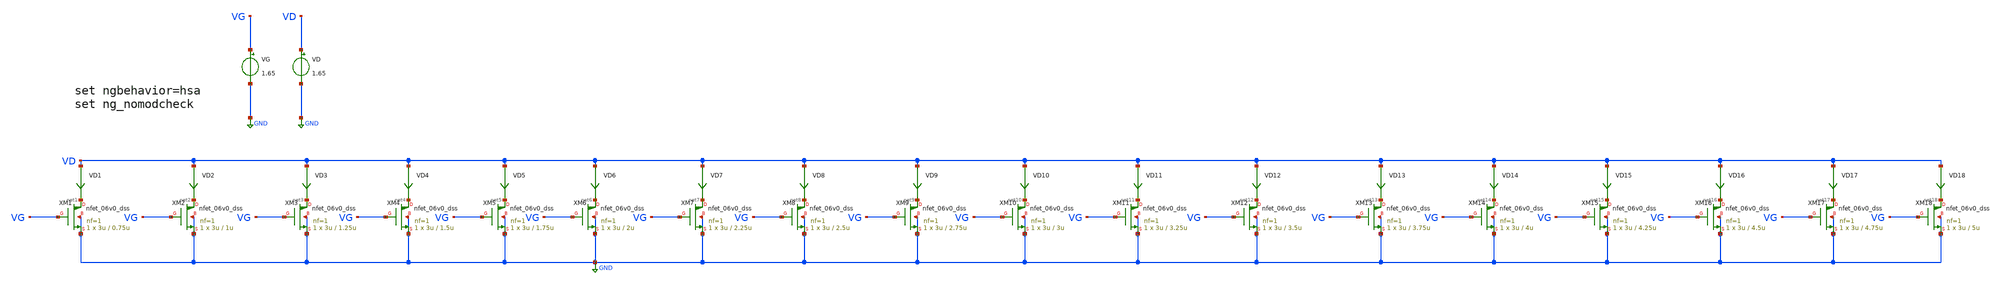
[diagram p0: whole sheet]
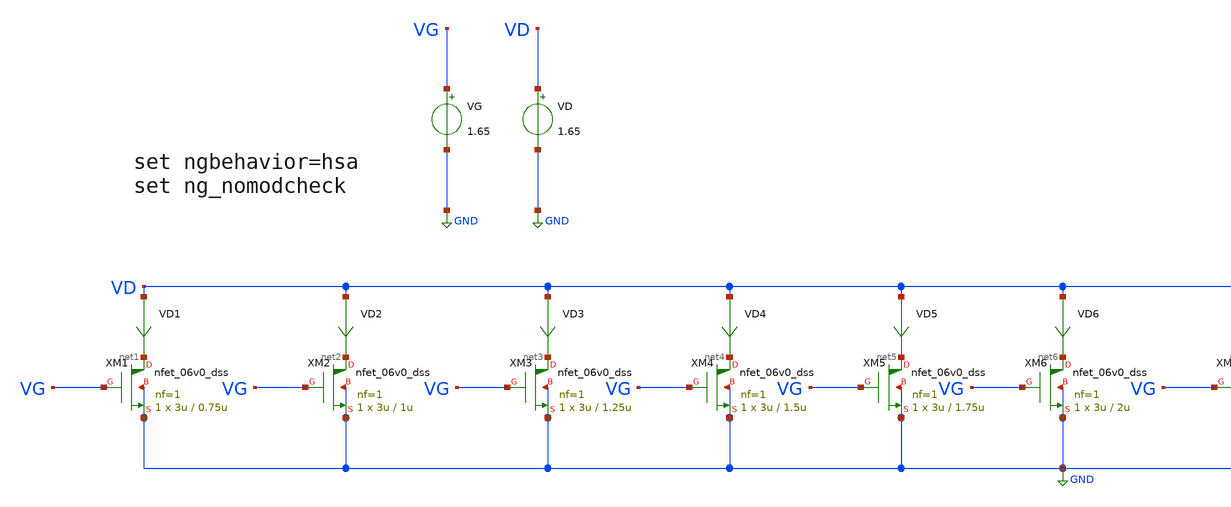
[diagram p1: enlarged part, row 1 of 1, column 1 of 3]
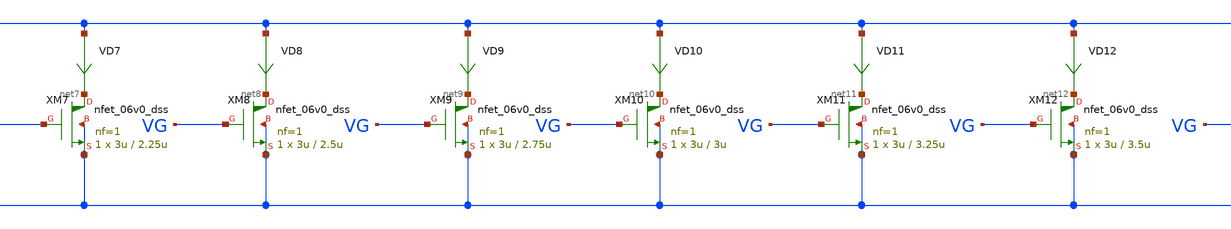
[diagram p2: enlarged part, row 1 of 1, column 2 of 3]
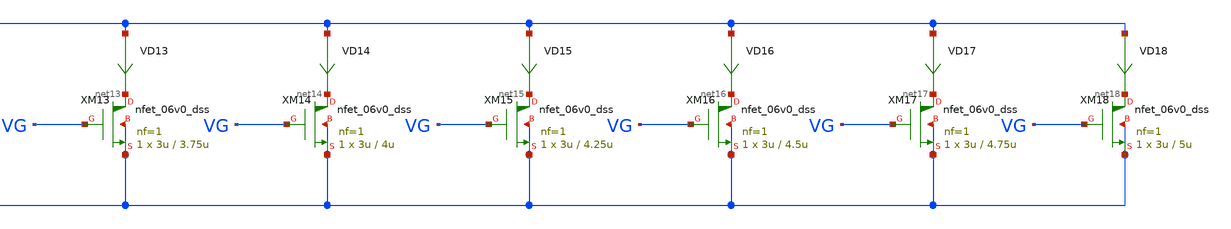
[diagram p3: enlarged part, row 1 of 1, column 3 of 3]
** sch_path: Design-Files/gmid_nmos_06v0_dss.sch
**.subckt gmid_nmos_06v0_dss
VG VG GND 1.65
VD VD GND 1.65
VD1 VD net1 0
.save i(vd1)
VD2 VD net2 0
.save i(vd2)
VD3 VD net3 0
.save i(vd3)
VD4 VD net4 0
.save i(vd4)
VD5 VD net5 0
.save i(vd5)
VD6 VD net6 0
.save i(vd6)
VD7 VD net7 0
.save i(vd7)
VD8 VD net8 0
.save i(vd8)
VD9 VD net9 0
.save i(vd9)
VD10 VD net10 0
.save i(vd10)
VD11 VD net11 0
.save i(vd11)
VD12 VD net12 0
.save i(vd12)
XM1 net1 VG GND GND nfet_06v0_dss L=0.75u W=3u nf=1 ad='int((nf+1)/2) * W/nf * 0.18u' as='int((nf+2)/2) * W/nf * 0.18u'
+ pd='2*int((nf+1)/2) * (W/nf + 0.18u)' ps='2*int((nf+2)/2) * (W/nf + 0.18u)' nrd='0.18u / W' nrs='0.18u / W'
+ sa=0 sb=0 sd=0 m=1
XM2 net2 VG GND GND nfet_06v0_dss L=1u W=3u nf=1 ad='int((nf+1)/2) * W/nf * 0.18u' as='int((nf+2)/2) * W/nf * 0.18u'
+ pd='2*int((nf+1)/2) * (W/nf + 0.18u)' ps='2*int((nf+2)/2) * (W/nf + 0.18u)' nrd='0.18u / W' nrs='0.18u / W'
+ sa=0 sb=0 sd=0 m=1
XM3 net3 VG GND GND nfet_06v0_dss L=1.25u W=3u nf=1 ad='int((nf+1)/2) * W/nf * 0.18u' as='int((nf+2)/2) * W/nf * 0.18u'
+ pd='2*int((nf+1)/2) * (W/nf + 0.18u)' ps='2*int((nf+2)/2) * (W/nf + 0.18u)' nrd='0.18u / W' nrs='0.18u / W'
+ sa=0 sb=0 sd=0 m=1
XM4 net4 VG GND GND nfet_06v0_dss L=1.5u W=3u nf=1 ad='int((nf+1)/2) * W/nf * 0.18u' as='int((nf+2)/2) * W/nf * 0.18u'
+ pd='2*int((nf+1)/2) * (W/nf + 0.18u)' ps='2*int((nf+2)/2) * (W/nf + 0.18u)' nrd='0.18u / W' nrs='0.18u / W'
+ sa=0 sb=0 sd=0 m=1
XM5 net5 VG GND GND nfet_06v0_dss L=1.75u W=3u nf=1 ad='int((nf+1)/2) * W/nf * 0.18u' as='int((nf+2)/2) * W/nf * 0.18u'
+ pd='2*int((nf+1)/2) * (W/nf + 0.18u)' ps='2*int((nf+2)/2) * (W/nf + 0.18u)' nrd='0.18u / W' nrs='0.18u / W'
+ sa=0 sb=0 sd=0 m=1
XM6 net6 VG GND GND nfet_06v0_dss L=2u W=3u nf=1 ad='int((nf+1)/2) * W/nf * 0.18u' as='int((nf+2)/2) * W/nf * 0.18u'
+ pd='2*int((nf+1)/2) * (W/nf + 0.18u)' ps='2*int((nf+2)/2) * (W/nf + 0.18u)' nrd='0.18u / W' nrs='0.18u / W'
+ sa=0 sb=0 sd=0 m=1
XM7 net7 VG GND GND nfet_06v0_dss L=2.25u W=3u nf=1 ad='int((nf+1)/2) * W/nf * 0.18u' as='int((nf+2)/2) * W/nf * 0.18u'
+ pd='2*int((nf+1)/2) * (W/nf + 0.18u)' ps='2*int((nf+2)/2) * (W/nf + 0.18u)' nrd='0.18u / W' nrs='0.18u / W'
+ sa=0 sb=0 sd=0 m=1
XM8 net8 VG GND GND nfet_06v0_dss L=2.5u W=3u nf=1 ad='int((nf+1)/2) * W/nf * 0.18u' as='int((nf+2)/2) * W/nf * 0.18u'
+ pd='2*int((nf+1)/2) * (W/nf + 0.18u)' ps='2*int((nf+2)/2) * (W/nf + 0.18u)' nrd='0.18u / W' nrs='0.18u / W'
+ sa=0 sb=0 sd=0 m=1
XM9 net9 VG GND GND nfet_06v0_dss L=2.75u W=3u nf=1 ad='int((nf+1)/2) * W/nf * 0.18u' as='int((nf+2)/2) * W/nf * 0.18u'
+ pd='2*int((nf+1)/2) * (W/nf + 0.18u)' ps='2*int((nf+2)/2) * (W/nf + 0.18u)' nrd='0.18u / W' nrs='0.18u / W'
+ sa=0 sb=0 sd=0 m=1
XM10 net10 VG GND GND nfet_06v0_dss L=3u W=3u nf=1 ad='int((nf+1)/2) * W/nf * 0.18u' as='int((nf+2)/2) * W/nf * 0.18u'
+ pd='2*int((nf+1)/2) * (W/nf + 0.18u)' ps='2*int((nf+2)/2) * (W/nf + 0.18u)' nrd='0.18u / W' nrs='0.18u / W'
+ sa=0 sb=0 sd=0 m=1
XM11 net11 VG GND GND nfet_06v0_dss L=3.25u W=3u nf=1 ad='int((nf+1)/2) * W/nf * 0.18u' as='int((nf+2)/2) * W/nf * 0.18u'
+ pd='2*int((nf+1)/2) * (W/nf + 0.18u)' ps='2*int((nf+2)/2) * (W/nf + 0.18u)' nrd='0.18u / W' nrs='0.18u / W'
+ sa=0 sb=0 sd=0 m=1
XM12 net12 VG GND GND nfet_06v0_dss L=3.5u W=3u nf=1 ad='int((nf+1)/2) * W/nf * 0.18u' as='int((nf+2)/2) * W/nf * 0.18u'
+ pd='2*int((nf+1)/2) * (W/nf + 0.18u)' ps='2*int((nf+2)/2) * (W/nf + 0.18u)' nrd='0.18u / W' nrs='0.18u / W'
+ sa=0 sb=0 sd=0 m=1
VD13 VD net13 0
.save i(vd13)
VD14 VD net14 0
.save i(vd14)
VD15 VD net15 0
.save i(vd15)
VD16 VD net16 0
.save i(vd16)
VD17 VD net17 0
.save i(vd17)
VD18 VD net18 0
.save i(vd18)
XM13 net13 VG GND GND nfet_06v0_dss L=3.75u W=3u nf=1 ad='int((nf+1)/2) * W/nf * 0.18u' as='int((nf+2)/2) * W/nf * 0.18u'
+ pd='2*int((nf+1)/2) * (W/nf + 0.18u)' ps='2*int((nf+2)/2) * (W/nf + 0.18u)' nrd='0.18u / W' nrs='0.18u / W'
+ sa=0 sb=0 sd=0 m=1
XM14 net14 VG GND GND nfet_06v0_dss L=4u W=3u nf=1 ad='int((nf+1)/2) * W/nf * 0.18u' as='int((nf+2)/2) * W/nf * 0.18u'
+ pd='2*int((nf+1)/2) * (W/nf + 0.18u)' ps='2*int((nf+2)/2) * (W/nf + 0.18u)' nrd='0.18u / W' nrs='0.18u / W'
+ sa=0 sb=0 sd=0 m=1
XM15 net15 VG GND GND nfet_06v0_dss L=4.25u W=3u nf=1 ad='int((nf+1)/2) * W/nf * 0.18u' as='int((nf+2)/2) * W/nf * 0.18u'
+ pd='2*int((nf+1)/2) * (W/nf + 0.18u)' ps='2*int((nf+2)/2) * (W/nf + 0.18u)' nrd='0.18u / W' nrs='0.18u / W'
+ sa=0 sb=0 sd=0 m=1
XM16 net16 VG GND GND nfet_06v0_dss L=4.5u W=3u nf=1 ad='int((nf+1)/2) * W/nf * 0.18u' as='int((nf+2)/2) * W/nf * 0.18u'
+ pd='2*int((nf+1)/2) * (W/nf + 0.18u)' ps='2*int((nf+2)/2) * (W/nf + 0.18u)' nrd='0.18u / W' nrs='0.18u / W'
+ sa=0 sb=0 sd=0 m=1
XM17 net17 VG GND GND nfet_06v0_dss L=4.75u W=3u nf=1 ad='int((nf+1)/2) * W/nf * 0.18u' as='int((nf+2)/2) * W/nf * 0.18u'
+ pd='2*int((nf+1)/2) * (W/nf + 0.18u)' ps='2*int((nf+2)/2) * (W/nf + 0.18u)' nrd='0.18u / W' nrs='0.18u / W'
+ sa=0 sb=0 sd=0 m=1
XM18 net18 VG GND GND nfet_06v0_dss L=5u W=3u nf=1 ad='int((nf+1)/2) * W/nf * 0.18u' as='int((nf+2)/2) * W/nf * 0.18u'
+ pd='2*int((nf+1)/2) * (W/nf + 0.18u)' ps='2*int((nf+2)/2) * (W/nf + 0.18u)' nrd='0.18u / W' nrs='0.18u / W'
+ sa=0 sb=0 sd=0 m=1
**** begin user architecture code


* ngspice commands
.option wnflag=1
.option .savecurrents
.control
save all
dc VG 0.05 6 0.1m
** remove zero length vectors to prevent write errors
remzerovec
write /foss/designs/PDK-CHAR/GF180-MCUD/NMOS_06v6_DSS/gmid_nmos_03v3_dss_tb.raw

plot @m.xm1.m0[gm]
plot @m.xm2.m0[gm]
plot @m.xm3.m0[gm]
plot @m.xm4.m0[gm]
plot @m.xm5.m0[gm]
plot @m.xm6.m0[gm]
plot @m.xm7.m0[gm]
plot @m.xm8.m0[gm]
plot @m.xm9.m0[gm]
plot @m.xm10.m0[gm]
plot @m.xm11.m0[gm]
plot @m.xm12.m0[gm]
plot @m.xm13.m0[gm]
plot @m.xm14.m0[gm]
plot @m.xm15.m0[gm]
plot @m.xm16.m0[gm]
plot @m.xm17.m0[gm]
plot @m.xm18.m0[gm]


wrdata /foss/designs/PDK-CHAR/GF180-MCUD/NMOS_06v0_DSS/gmid_nmos_1_nfet_03v3_dss_tb.txt
+ @m.xm1.m0[gm] i(VD1) @m.xm1.m0[vth] @m.xm1.m0[gds] @m.xm1.m0[cgg] @m.xm1.m0[cgs] @m.xm1.m0[cgd]
wrdata /foss/designs/PDK-CHAR/GF180-MCUD/NMOS_06v0_DSS/gmid_nmos_2_nfet_03v3_dss_tb.txt
+ @m.xm2.m0[gm] i(VD2) @m.xm2.m0[vth] @m.xm2.m0[gds] @m.xm2.m0[cgg] @m.xm2.m0[cgs] @m.xm2.m0[cgd]
wrdata /foss/designs/PDK-CHAR/GF180-MCUD/NMOS_06v0_DSS/gmid_nmos_3_nfet_03v3_dss_tb.txt
+ @m.xm3.m0[gm] i(VD3) @m.xm3.m0[vth] @m.xm3.m0[gds] @m.xm3.m0[cgg] @m.xm3.m0[cgs] @m.xm3.m0[cgd]
wrdata /foss/designs/PDK-CHAR/GF180-MCUD/NMOS_06v0_DSS/gmid_nmos_4_nfet_03v3_dss_tb.txt
+ @m.xm4.m0[gm] i(VD4) @m.xm4.m0[vth] @m.xm4.m0[gds] @m.xm4.m0[cgg] @m.xm4.m0[cgs] @m.xm4.m0[cgd]
wrdata /foss/designs/PDK-CHAR/GF180-MCUD/NMOS_06v0_DSS/gmid_nmos_5_nfet_03v3_dss_tb.txt
+ @m.xm5.m0[gm] i(VD5) @m.xm5.m0[vth] @m.xm5.m0[gds] @m.xm5.m0[cgg] @m.xm5.m0[cgs] @m.xm5.m0[cgd]
wrdata /foss/designs/PDK-CHAR/GF180-MCUD/NMOS_06v0_DSS/gmid_nmos_6_nfet_03v3_dss_tb.txt
+ @m.xm6.m0[gm] i(VD6) @m.xm6.m0[vth] @m.xm6.m0[gds] @m.xm6.m0[cgg] @m.xm6.m0[cgs] @m.xm6.m0[cgd]
wrdata /foss/designs/PDK-CHAR/GF180-MCUD/NMOS_06v0_DSS/gmid_nmos_7_nfet_03v3_dss_tb.txt
+ @m.xm7.m0[gm] i(VD7) @m.xm7.m0[vth] @m.xm7.m0[gds] @m.xm7.m0[cgg] @m.xm7.m0[cgs] @m.xm7.m0[cgd]
wrdata /foss/designs/PDK-CHAR/GF180-MCUD/NMOS_06v0_DSS/gmid_nmos_8_nfet_03v3_dss_tb.txt
+ @m.xm8.m0[gm] i(VD8) @m.xm8.m0[vth] @m.xm8.m0[gds] @m.xm8.m0[cgg] @m.xm8.m0[cgs] @m.xm8.m0[cgd]
wrdata /foss/designs/PDK-CHAR/GF180-MCUD/NMOS_06v0_DSS/gmid_nmos_9_nfet_03v3_dss_tb.txt
+ @m.xm9.m0[gm] i(VD9) @m.xm9.m0[vth] @m.xm9.m0[gds] @m.xm9.m0[cgg] @m.xm9.m0[cgs] @m.xm9.m0[cgd]
wrdata /foss/designs/PDK-CHAR/GF180-MCUD/NMOS_06v0_DSS/gmid_nmos_10_nfet_03v3_dss_tb.txt
+ @m.xm10.m0[gm] i(VD10) @m.xm10.m0[vth] @m.xm10.m0[gds] @m.xm10.m0[cgg] @m.xm10.m0[cgs] @m.xm10.m0[cgd]
wrdata /foss/designs/PDK-CHAR/GF180-MCUD/NMOS_06v0_DSS/gmid_nmos_11_nfet_03v3_dss_tb.txt
+ @m.xm11.m0[gm] i(VD11) @m.xm11.m0[vth] @m.xm11.m0[gds] @m.xm11.m0[cgg] @m.xm11.m0[cgs] @m.xm11.m0[cgd]
wrdata /foss/designs/PDK-CHAR/GF180-MCUD/NMOS_06v0_DSS/gmid_nmos_12_nfet_03v3_dss_tb.txt
+ @m.xm12.m0[gm] i(VD12) @m.xm12.m0[vth] @m.xm12.m0[gds] @m.xm12.m0[cgg] @m.xm12.m0[cgs] @m.xm12.m0[cgd]
wrdata /foss/designs/PDK-CHAR/GF180-MCUD/NMOS_06v0_DSS/gmid_nmos_13_nfet_03v3_dss_tb.txt
+ @m.xm13.m0[gm] i(VD13) @m.xm13.m0[vth] @m.xm13.m0[gds] @m.xm13.m0[cgg] @m.xm13.m0[cgs] @m.xm13.m0[cgd]
wrdata /foss/designs/PDK-CHAR/GF180-MCUD/NMOS_06v0_DSS/gmid_nmos_14_nfet_03v3_dss_tb.txt
+ @m.xm14.m0[gm] i(VD14) @m.xm14.m0[vth] @m.xm14.m0[gds] @m.xm14.m0[cgg] @m.xm14.m0[cgs] @m.xm14.m0[cgd]
wrdata /foss/designs/PDK-CHAR/GF180-MCUD/NMOS_06v0_DSS/gmid_nmos_15_nfet_03v3_dss_tb.txt
+ @m.xm15.m0[gm] i(VD15) @m.xm15.m0[vth] @m.xm15.m0[gds] @m.xm15.m0[cgg] @m.xm15.m0[cgs] @m.xm15.m0[cgd]
wrdata /foss/designs/PDK-CHAR/GF180-MCUD/NMOS_06v0_DSS/gmid_nmos_16_nfet_03v3_dss_tb.txt
+ @m.xm16.m0[gm] i(VD13) @m.xm16.m0[vth] @m.xm16.m0[gds] @m.xm16.m0[cgg] @m.xm16.m0[cgs] @m.xm16.m0[cgd]
wrdata /foss/designs/PDK-CHAR/GF180-MCUD/NMOS_06v0_DSS/gmid_nmos_17_nfet_03v3_dss_tb.txt
+ @m.xm17.m0[gm] i(VD14) @m.xm17.m0[vth] @m.xm17.m0[gds] @m.xm17.m0[cgg] @m.xm17.m0[cgs] @m.xm17.m0[cgd]
wrdata /foss/designs/PDK-CHAR/GF180-MCUD/NMOS_06v0_DSS/gmid_nmos_18_nfet_03v3_dss_tb.txt
+ @m.xm18.m0[gm] i(VD15) @m.xm18.m0[vth] @m.xm18.m0[gds] @m.xm18.m0[cgg] @m.xm18.m0[cgs] @m.xm18.m0[cgd]
set appendwrite
op
remzerovec
write /foss/designs/PDK-CHAR/GF180-MCUD/NMOS_06v6_DSS/gmid_nmos_03v3_dss_tb.raw
**quit 0
.endc




.save @m.xm1.m0[gm]
.save @m.xm1.m0[vth]
.save @m.xm1.m0[gds]
.save @m.xm1.m0[cgg]
.save @m.xm1.m0[cgs]
.save @m.xm1.m0[cgd]
.save @m.xm2.m0[gm]
.save @m.xm2.m0[vth]
.save @m.xm2.m0[gds]
.save @m.xm2.m0[cgg]
.save @m.xm2.m0[cgs]
.save @m.xm2.m0[cgd]
.save @m.xm3.m0[gm]
.save @m.xm3.m0[vth]
.save @m.xm3.m0[gds]
.save @m.xm3.m0[cgg]
.save @m.xm3.m0[cgs]
.save @m.xm3.m0[cgd]
.save @m.xm4.m0[gm]
.save @m.xm4.m0[vth]
.save @m.xm4.m0[gds]
.save @m.xm4.m0[cgg]
.save @m.xm4.m0[cgs]
.save @m.xm4.m0[cgd]
.save @m.xm5.m0[gm]
.save @m.xm5.m0[vth]
.save @m.xm5.m0[gds]
.save @m.xm5.m0[cgg]
.save @m.xm5.m0[cgs]
.save @m.xm5.m0[cgd]
.save @m.xm6.m0[gm]
.save @m.xm6.m0[vth]
.save @m.xm6.m0[gds]
.save @m.xm6.m0[cgg]
.save @m.xm6.m0[cgs]
.save @m.xm6.m0[cgd]
.save @m.xm7.m0[gm]
.save @m.xm7.m0[vth]
.save @m.xm7.m0[gds]
.save @m.xm7.m0[cgg]
.save @m.xm7.m0[cgs]
.save @m.xm7.m0[cgd]
.save @m.xm8.m0[gm]
.save @m.xm8.m0[vth]
.save @m.xm8.m0[gds]
.save @m.xm8.m0[cgg]
.save @m.xm8.m0[cgs]
.save @m.xm8.m0[cgd]
.save @m.xm9.m0[gm]
.save @m.xm9.m0[vth]
.save @m.xm9.m0[gds]
.save @m.xm9.m0[cgg]
.save @m.xm9.m0[cgs]
.save @m.xm9.m0[cgd]
.save @m.xm10.m0[gm]
.save @m.xm10.m0[vth]
.save @m.xm10.m0[gds]
.save @m.xm10.m0[cgg]
.save @m.xm10.m0[cgs]
.save @m.xm10.m0[cgd]
.save @m.xm11.m0[gm]
.save @m.xm11.m0[vth]
.save @m.xm11.m0[gds]
.save @m.xm11.m0[cgg]
.save @m.xm11.m0[cgs]
.save @m.xm11.m0[cgd]
.save @m.xm12.m0[gm]
.save @m.xm12.m0[vth]
.save @m.xm12.m0[gds]
.save @m.xm12.m0[cgg]
.save @m.xm12.m0[cgs]
.save @m.xm12.m0[cgd]
.save @m.xm13.m0[gm]
.save @m.xm13.m0[vth]
.save @m.xm13.m0[gds]
.save @m.xm13.m0[cgg]
.save @m.xm13.m0[cgs]
.save @m.xm13.m0[cgd]
.save @m.xm14.m0[gm]
.save @m.xm14.m0[vth]
.save @m.xm14.m0[gds]
.save @m.xm14.m0[cgg]
.save @m.xm14.m0[cgs]
.save @m.xm14.m0[cgd]
.save @m.xm15.m0[gm]
.save @m.xm15.m0[vth]
.save @m.xm15.m0[gds]
.save @m.xm15.m0[cgg]
.save @m.xm15.m0[cgs]
.save @m.xm15.m0[cgd]
.save @m.xm16.m0[gm]
.save @m.xm16.m0[vth]
.save @m.xm16.m0[gds]
.save @m.xm16.m0[cgg]
.save @m.xm16.m0[cgs]
.save @m.xm16.m0[cgd]
.save @m.xm17.m0[gm]
.save @m.xm17.m0[vth]
.save @m.xm17.m0[gds]
.save @m.xm17.m0[cgg]
.save @m.xm17.m0[cgs]
.save @m.xm17.m0[cgd]
.save @m.xm18.m0[gm]
.save @m.xm18.m0[vth]
.save @m.xm18.m0[gds]
.save @m.xm18.m0[cgg]
.save @m.xm18.m0[cgs]
.save @m.xm18.m0[cgd]




.lib /foss/pdks/volare/gf180mcu/versions/0fe599b2afb6708d281543108caf8310912f54af/gf180mcuD/libs.tech/ngspice/sm141064.ngspice typical
.include /foss/pdks/volare/gf180mcu/versions/0fe599b2afb6708d281543108caf8310912f54af/gf180mcuD/libs.tech/ngspice/design.ngspice

*.include $::180MCU_MODELS/design.ngspice
*.lib $::180MCU_MODELS/sm141064.ngspice typical


**** end user architecture code
**.ends
.GLOBAL GND
.end
